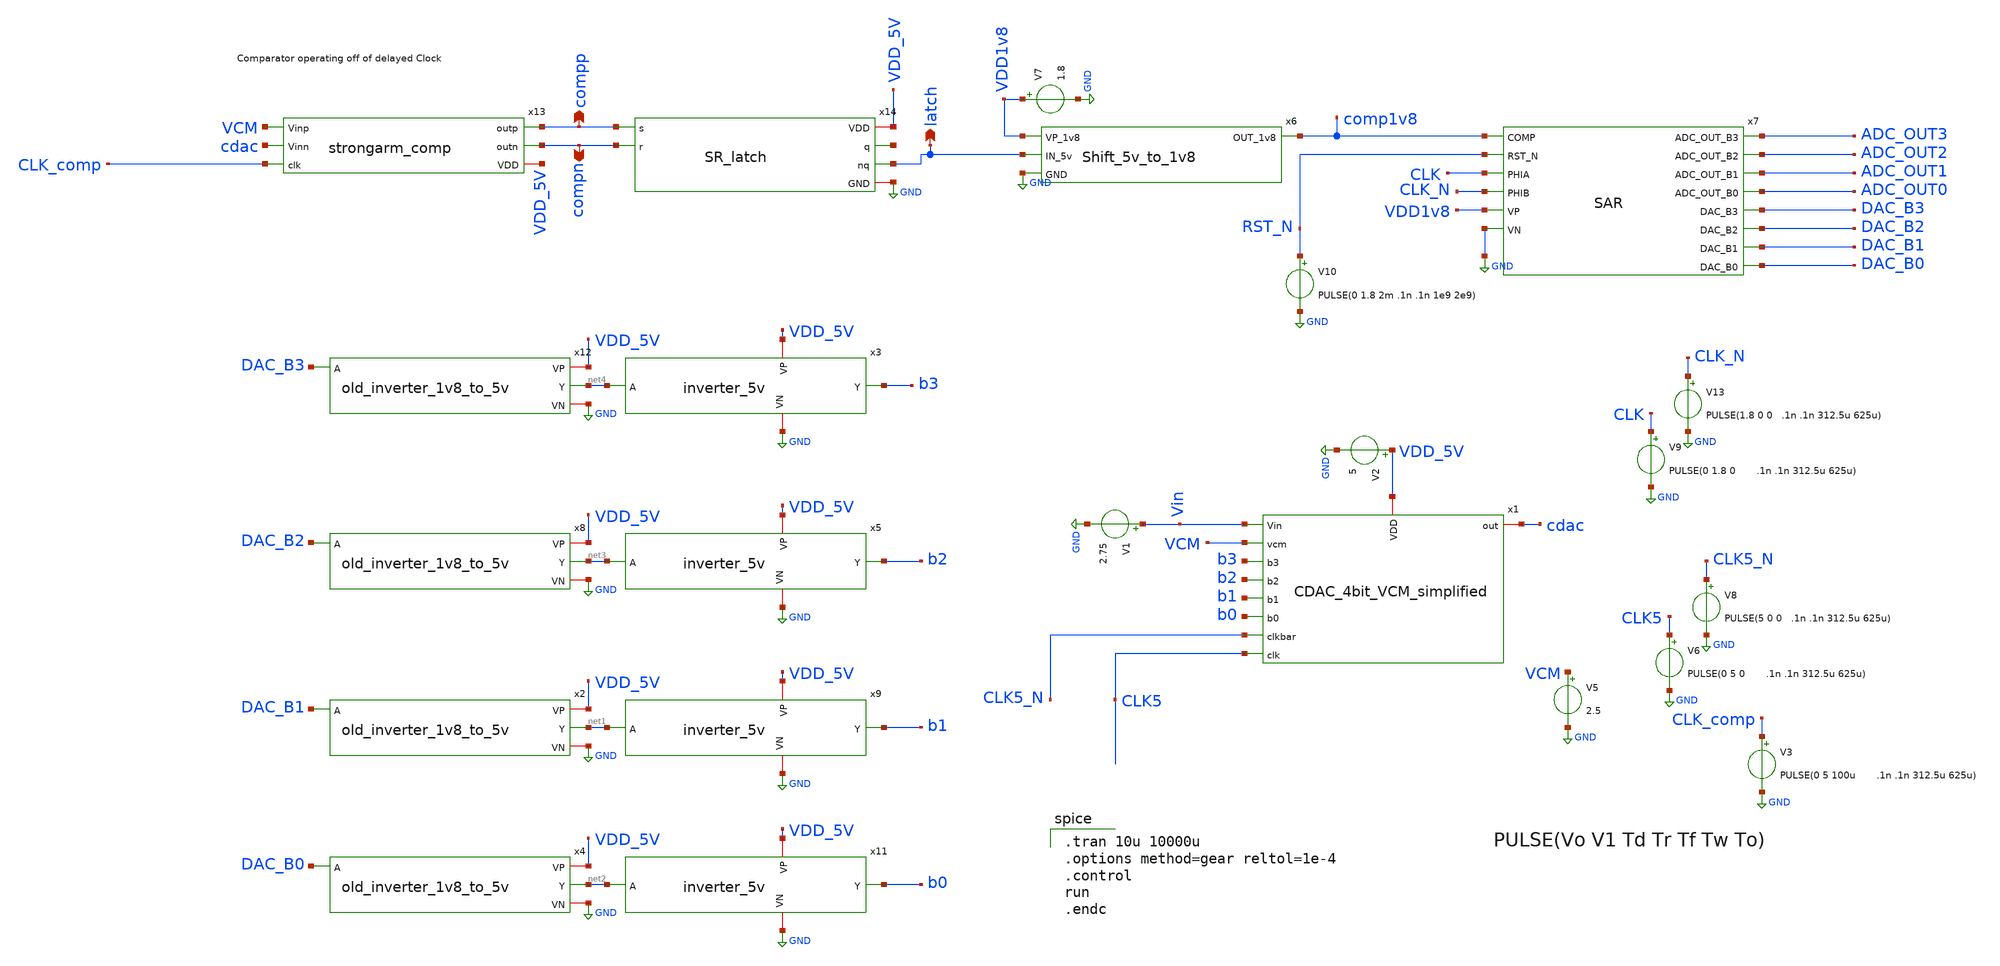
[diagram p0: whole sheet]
** sch_path: ADC/4bit_C2C/MagicAndSpice/old_CDAC_4bit_VCM_simplified_TB_inverter_test2_apr19_clkdelaycomp_invimprove.sch
**.subckt old_CDAC_4bit_VCM_simplified_TB_inverter_test2_apr19_clkdelaycomp_invimprove compp latch
*+ compn
*.opin compp
*.opin latch
*.opin compn
V2 VDD_5V GND 5
V1 Vin GND 2.75
V5 VCM GND 2.5
x1 CLK5_N CLK5 Vin b3 b0 b2 b1 VCM cdac VDD_5V CDAC_4bit_VCM_simplified
x3 VDD_5V net4 b3 GND inverter_5v
x5 VDD_5V net3 b2 GND inverter_5v
x9 VDD_5V net1 b1 GND inverter_5v
x11 VDD_5V net2 b0 GND inverter_5v
V7 VDD1v8 GND 1.8
x6 VDD1v8 comp1v8 latch GND Shift_5v_to_1v8
V10 RST_N GND PULSE(0 1.8 2m .1n .1n 1e9 2e9)
x7 comp1v8 RST_N CLK CLK_N ADC_OUT3 ADC_OUT2 ADC_OUT1 ADC_OUT0 DAC_B3 DAC_B2 DAC_B1 DAC_B0 VDD1v8
+ GND SAR
x13 compp compn VCM cdac VDD_5V CLK_comp strongarm_comp
x14 VDD_5V net5 compp latch compn GND SR_latch
V6 CLK5 GND PULSE(0 5 0 .1n .1n 312.5u 625u)
V8 CLK5_N GND PULSE(5 0 0 .1n .1n 312.5u 625u)
V9 CLK GND PULSE(0 1.8 0 .1n .1n 312.5u 625u)
V13 CLK_N GND PULSE(1.8 0 0 .1n .1n 312.5u 625u)
V3 CLK_comp GND PULSE(0 5 100u .1n .1n 312.5u 625u)
x2 VDD_5V DAC_B1 net1 GND old_inverter_1v8_to_5v
x4 VDD_5V DAC_B0 net2 GND old_inverter_1v8_to_5v
x8 VDD_5V DAC_B2 net3 GND old_inverter_1v8_to_5v
x12 VDD_5V DAC_B3 net4 GND old_inverter_1v8_to_5v
**** begin user architecture code

** opencircuitdesign pdks install
.lib $::SKYWATER_MODELS/sky130.lib.spice tt



.tran 10u 10000u
.options method=gear reltol=1e-4
.control
run
.endc

**** end user architecture code
**.ends
.GLOBAL GND
.end
